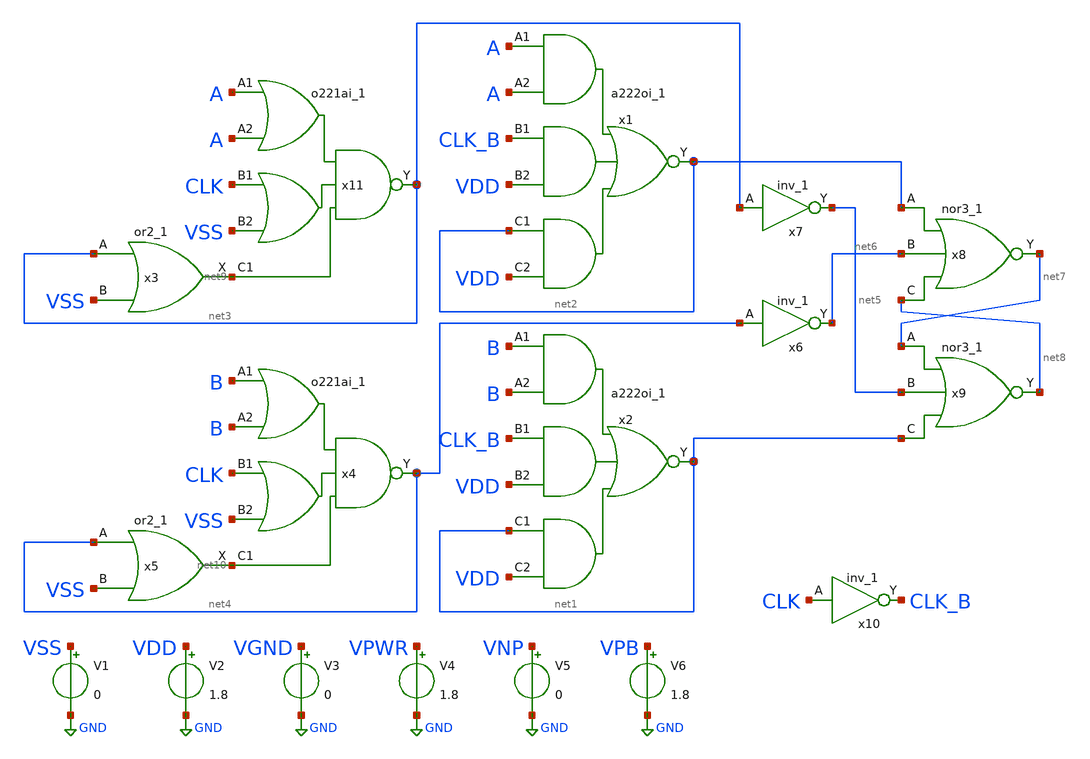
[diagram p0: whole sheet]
** sch_path: analog comparator/AOI-OAI-based_comp/schematics/AOI-OAI_comp.sch
**.subckt AOI-OAI_comp
x1 A A CLK_B VDD net2 VDD VGND VNB VPB VPWR net2 sky130_fd_sc_hd__a222oi_1
x2 B B CLK_B VDD net1 VDD VGND VNB VPB VPWR net1 sky130_fd_sc_hd__a222oi_1
V1 VSS GND 0
V2 VDD GND 1.8
V3 VGND GND 0
V4 VPWR GND 1.8
V5 VNP GND 0
V6 VPB GND 1.8
x11 A A CLK VSS net9 VGND VNB VPB VPWR net3 sky130_fd_sc_hd__o221ai_1
x3 net3 VSS VGND VNB VPB VPWR net9 sky130_fd_sc_hd__or2_1
x4 B B CLK VSS net10 VGND VNB VPB VPWR net4 sky130_fd_sc_hd__o221ai_1
x5 net4 VSS VGND VNB VPB VPWR net10 sky130_fd_sc_hd__or2_1
x6 net4 VGND VNB VPB VPWR net6 sky130_fd_sc_hd__inv_1
x7 net3 VGND VNB VPB VPWR net5 sky130_fd_sc_hd__inv_1
x8 net2 net6 net8 VGND VNB VPB VPWR net7 sky130_fd_sc_hd__nor3_1
x9 net7 net5 net1 VGND VNB VPB VPWR net8 sky130_fd_sc_hd__nor3_1
x10 CLK VGND VNB VPB VPWR CLK_B sky130_fd_sc_hd__inv_1
**.ends
.GLOBAL GND
.end
